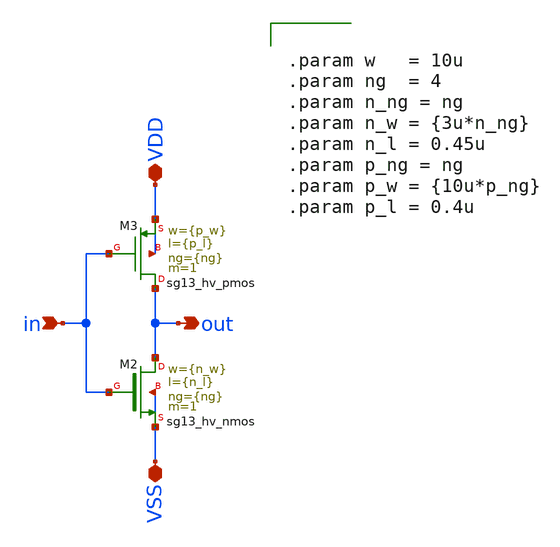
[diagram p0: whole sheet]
** sch_path: macros/heichips26_vcr/macros/switched_capacitor/schematic/xschem/hv_inverter_40u.sch
**.subckt hv_inverter_40u in VDD VSS out
*.ipin in
*.iopin VDD
*.iopin VSS
*.opin out
XM2 out in VSS VSS sg13_hv_nmos w={n_w} l={n_l} ng={ng} m=1 mm_ok=1
XM3 out in VDD VDD sg13_hv_pmos w={p_w} l={p_l} ng={ng} m=1 mm_ok=1
**** begin user architecture code


.param w   = 10u
.param ng  = 4
.param n_ng = ng
.param n_w = {3u*n_ng}
.param n_l = 0.45u
.param p_ng = ng
.param p_w = {10u*p_ng}
.param p_l = 0.4u


**** end user architecture code
**.ends
.end
